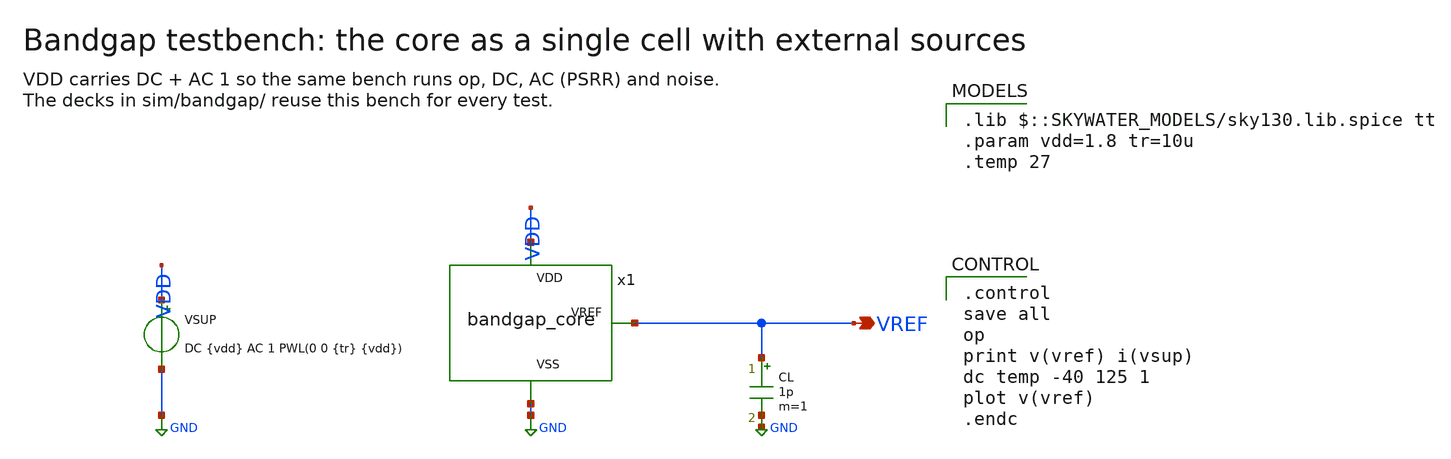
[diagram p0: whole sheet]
** sch_path: xschem/bandgap_tb.sch
**.subckt bandgap_tb VREF
*.opin VREF
VSUP VDD GND DC {vdd} AC 1 PWL(0 0 {tr} {vdd})
.save i(vsup)
x1 VDD GND VREF bandgap_core
CL VREF GND 1p m=1
**** begin user architecture code
 .lib $::SKYWATER_MODELS/sky130.lib.spice tt
.param vdd=1.8 tr=10u
.temp 27

.control
save all
op
print v(vref) i(vsup)
dc temp -40 125 1
plot v(vref)
.endc

**** end user architecture code
**.ends

* expanding   symbol:  bandgap_core.sym # of pins=3
** sym_path: xschem/bandgap_core.sym
** sch_path: xschem/bandgap_core.sch
.subckt bandgap_core VDD VSS VREF
*.opin VREF
*.iopin VDD
*.iopin VSS
XM9 S VSS VDD VDD sky130_fd_pr__pfet_01v8 L=8 W=0.42 nf=1 ad=0.1218 as=0.1218 pd=1.42 ps=1.42
+ nrd=0.6905 nrs=0.6905 sa=0 sb=0 sd=0 mult=1 m=1
XM10 S VREF VSS VSS sky130_fd_pr__nfet_01v8 L=1 W=1 nf=1 ad=0.29 as=0.29 pd=2.58 ps=2.58 nrd=0.29
+ nrs=0.29 sa=0 sb=0 sd=0 mult=1 m=1
XM11 PB S VSS VSS sky130_fd_pr__nfet_01v8 L=1 W=0.42 nf=1 ad=0.1218 as=0.1218 pd=1.42 ps=1.42
+ nrd=0.6905 nrs=0.6905 sa=0 sb=0 sd=0 mult=1 m=1
XM1 A PB VDD VDD sky130_fd_pr__pfet_01v8 L=4 W=8 nf=1 ad=2.32 as=2.32 pd=16.58 ps=16.58 nrd=0.0362
+ nrs=0.0362 sa=0 sb=0 sd=0 mult=1 m=1
XM2 B PB VDD VDD sky130_fd_pr__pfet_01v8 L=4 W=8 nf=1 ad=2.32 as=2.32 pd=16.58 ps=16.58 nrd=0.0362
+ nrs=0.0362 sa=0 sb=0 sd=0 mult=1 m=1
XM3 VREF PB VDD VDD sky130_fd_pr__pfet_01v8 L=4 W=8 nf=1 ad=2.32 as=2.32 pd=16.58 ps=16.58
+ nrd=0.0362 nrs=0.0362 sa=0 sb=0 sd=0 mult=1 m=1
XQ1 VSS VSS A sky130_fd_pr__pnp_05v5_W3p40L3p40 m=1
XR1 net1 B VSS sky130_fd_pr__res_xhigh_po_0p35 L=2 mult=1 m=1
XQ2 VSS VSS net1 sky130_fd_pr__pnp_05v5_W3p40L3p40 m=8
XR2 net2 VREF VSS sky130_fd_pr__res_xhigh_po_0p35 L=17.7 mult=1 m=1
XQ3 VSS VSS net2 sky130_fd_pr__pnp_05v5_W3p40L3p40 m=1
XM12 NB PB VDD VDD sky130_fd_pr__pfet_01v8 L=4 W=8 nf=1 ad=2.32 as=2.32 pd=16.58 ps=16.58 nrd=0.0362
+ nrs=0.0362 sa=0 sb=0 sd=0 mult=1 m=1
XM13 NB NB VSS VSS sky130_fd_pr__nfet_01v8 L=4 W=8 nf=1 ad=2.32 as=2.32 pd=16.58 ps=16.58 nrd=0.0362
+ nrs=0.0362 sa=0 sb=0 sd=0 mult=1 m=1
XM7 N1 N1 VDD VDD sky130_fd_pr__pfet_01v8 L=4 W=4 nf=1 ad=1.16 as=1.16 pd=8.58 ps=8.58 nrd=0.0725
+ nrs=0.0725 sa=0 sb=0 sd=0 mult=1 m=1
XM8 PBO N1 VDD VDD sky130_fd_pr__pfet_01v8 L=4 W=4 nf=1 ad=1.16 as=1.16 pd=8.58 ps=8.58 nrd=0.0725
+ nrs=0.0725 sa=0 sb=0 sd=0 mult=1 m=1
XM5 N1 B TAIL VSS sky130_fd_pr__nfet_01v8_lvt L=4 W=16 nf=1 ad=4.64 as=4.64 pd=32.58 ps=32.58
+ nrd=0.0181 nrs=0.0181 sa=0 sb=0 sd=0 mult=1 m=1
XM6 PBO A TAIL VSS sky130_fd_pr__nfet_01v8_lvt L=4 W=16 nf=1 ad=4.64 as=4.64 pd=32.58 ps=32.58
+ nrd=0.0181 nrs=0.0181 sa=0 sb=0 sd=0 mult=1 m=1
XM4 TAIL NB VSS VSS sky130_fd_pr__nfet_01v8 L=4 W=8 nf=1 ad=2.32 as=2.32 pd=16.58 ps=16.58
+ nrd=0.0362 nrs=0.0362 sa=0 sb=0 sd=0 mult=1 m=1
Vloop PB PBO 0
XC1 VDD PBO sky130_fd_pr__cap_mim_m3_1 W=30 L=30 MF=1 m=1
.ends

.GLOBAL GND
.end
